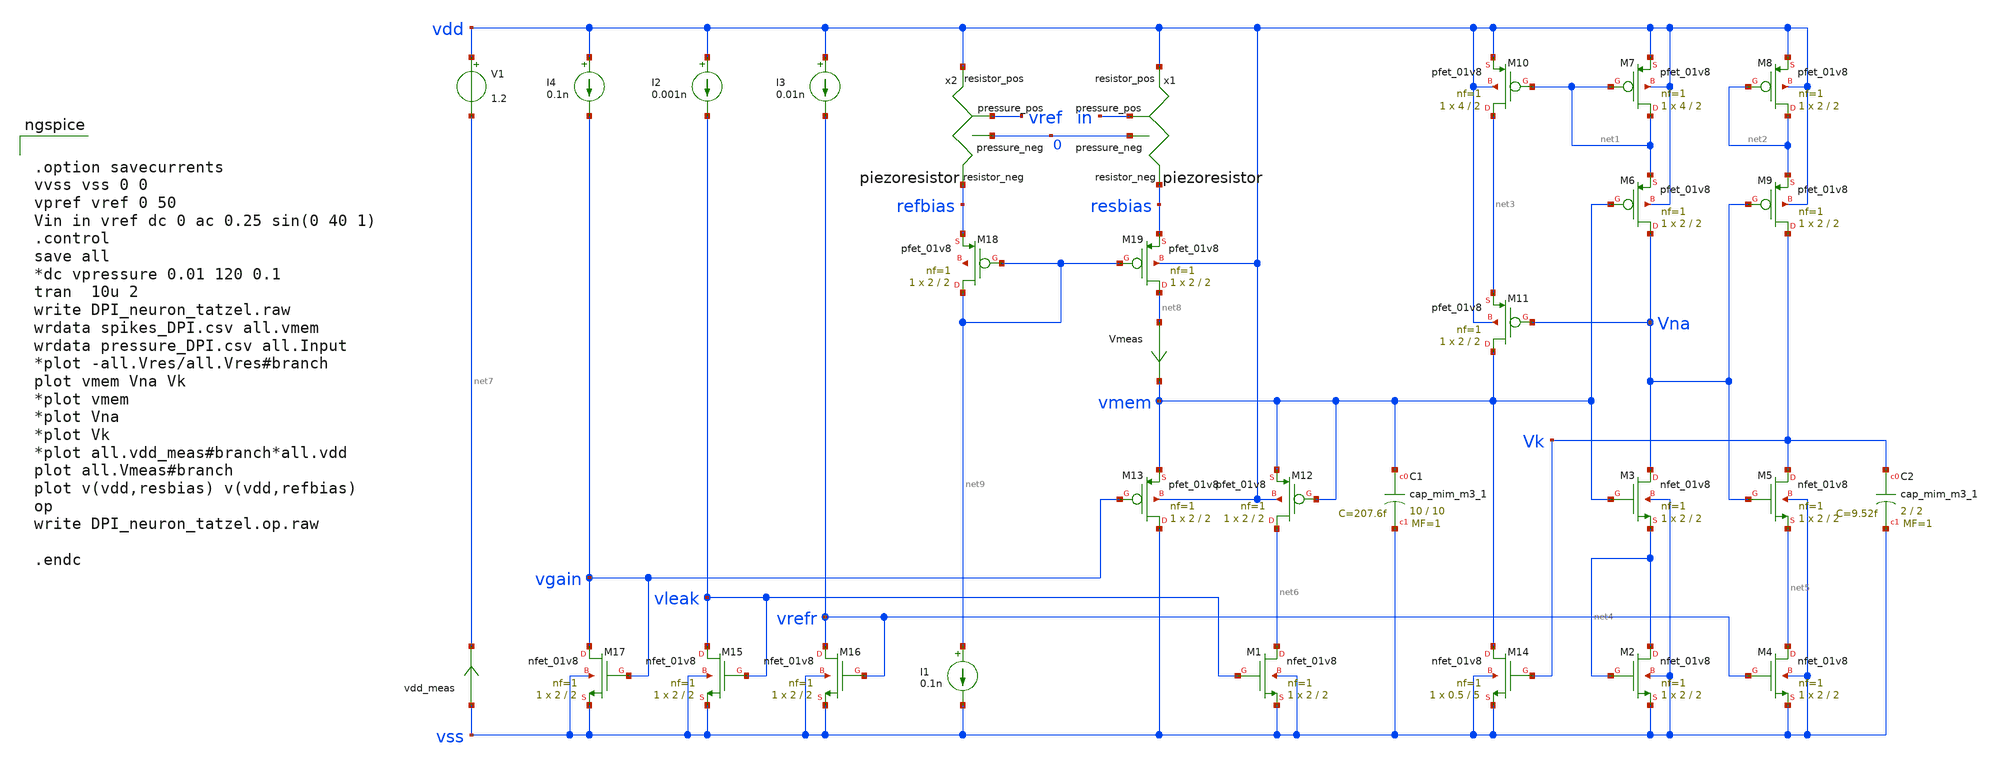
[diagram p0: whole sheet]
** sch_path: circuits/DPI_neuron_tatzel.sch
* Copyright 2020 Stefan Frederik Schippers
* Licensed under the Apache License, Version 2.0 (the "License");
* you may not use this file except in compliance with the License.
* You may obtain a copy of the License at
* https://www.apache.org/licenses/LICENSE-2.0
* Unless required by applicable law or agreed to in writing, software
* distributed under the License is distributed on an "AS IS" BASIS,
* WITHOUT WARRANTIES OR CONDITIONS OF ANY KIND, either express or implied.
* See the License for the specific language governing permissions and
* limitations under the License.
**.subckt DPI_neuron_tatzel
Vmeas net8 vmem 0
.save i(vmeas)
vdd_meas vss net7 0
.save i(vdd_meas)
V1 vdd net7 1.2
XM1 net6 vleak vss vss sky130_fd_pr__nfet_01v8 L=2 W=2 nf=1 ad='int((nf+1)/2) * W/nf * 0.29' as='int((nf+2)/2) * W/nf * 0.29'
+ pd='2*int((nf+1)/2) * (W/nf + 0.29)' ps='2*int((nf+2)/2) * (W/nf + 0.29)' nrd='0.29 / W' nrs='0.29 / W'
+ sa=0 sb=0 sd=0 mult=1 m=1
XM2 net4 net4 vss vss sky130_fd_pr__nfet_01v8 L=2 W=2 nf=1 ad='int((nf+1)/2) * W/nf * 0.29' as='int((nf+2)/2) * W/nf * 0.29'
+ pd='2*int((nf+1)/2) * (W/nf + 0.29)' ps='2*int((nf+2)/2) * (W/nf + 0.29)' nrd='0.29 / W' nrs='0.29 / W'
+ sa=0 sb=0 sd=0 mult=1 m=1
XM3 Vna vmem net4 vss sky130_fd_pr__nfet_01v8 L=2 W=2 nf=1 ad='int((nf+1)/2) * W/nf * 0.29' as='int((nf+2)/2) * W/nf * 0.29'
+ pd='2*int((nf+1)/2) * (W/nf + 0.29)' ps='2*int((nf+2)/2) * (W/nf + 0.29)' nrd='0.29 / W' nrs='0.29 / W'
+ sa=0 sb=0 sd=0 mult=1 m=1
XC1 vmem vss sky130_fd_pr__cap_mim_m3_1 W=10 L=10 MF=1 m=1
XC2 Vk vss sky130_fd_pr__cap_mim_m3_1 W=2 L=2 MF=1 m=1
XM14 vmem Vk vss vss sky130_fd_pr__nfet_01v8 L=5 W=0.5 nf=1 ad='int((nf+1)/2) * W/nf * 0.29' as='int((nf+2)/2) * W/nf * 0.29'
+ pd='2*int((nf+1)/2) * (W/nf + 0.29)' ps='2*int((nf+2)/2) * (W/nf + 0.29)' nrd='0.29 / W' nrs='0.29 / W'
+ sa=0 sb=0 sd=0 mult=1 m=1
XM4 net5 vrefr vss vss sky130_fd_pr__nfet_01v8 L=2 W=2 nf=1 ad='int((nf+1)/2) * W/nf * 0.29' as='int((nf+2)/2) * W/nf * 0.29'
+ pd='2*int((nf+1)/2) * (W/nf + 0.29)' ps='2*int((nf+2)/2) * (W/nf + 0.29)' nrd='0.29 / W' nrs='0.29 / W'
+ sa=0 sb=0 sd=0 mult=1 m=1
XM5 Vk Vna net5 vss sky130_fd_pr__nfet_01v8 L=2 W=2 nf=1 ad='int((nf+1)/2) * W/nf * 0.29' as='int((nf+2)/2) * W/nf * 0.29'
+ pd='2*int((nf+1)/2) * (W/nf + 0.29)' ps='2*int((nf+2)/2) * (W/nf + 0.29)' nrd='0.29 / W' nrs='0.29 / W'
+ sa=0 sb=0 sd=0 mult=1 m=1
I2 vdd vleak 0.001n
XM15 vleak vleak vss vss sky130_fd_pr__nfet_01v8 L=2 W=2 nf=1 ad='int((nf+1)/2) * W/nf * 0.29' as='int((nf+2)/2) * W/nf * 0.29'
+ pd='2*int((nf+1)/2) * (W/nf + 0.29)' ps='2*int((nf+2)/2) * (W/nf + 0.29)' nrd='0.29 / W' nrs='0.29 / W'
+ sa=0 sb=0 sd=0 mult=1 m=1
I3 vdd vrefr 0.01n
XM16 vrefr vrefr vss vss sky130_fd_pr__nfet_01v8 L=2 W=2 nf=1 ad='int((nf+1)/2) * W/nf * 0.29' as='int((nf+2)/2) * W/nf * 0.29'
+ pd='2*int((nf+1)/2) * (W/nf + 0.29)' ps='2*int((nf+2)/2) * (W/nf + 0.29)' nrd='0.29 / W' nrs='0.29 / W'
+ sa=0 sb=0 sd=0 mult=1 m=1
I4 vdd vgain 0.1n
XM17 vgain vgain vss vss sky130_fd_pr__nfet_01v8 L=2 W=2 nf=1 ad='int((nf+1)/2) * W/nf * 0.29' as='int((nf+2)/2) * W/nf * 0.29'
+ pd='2*int((nf+1)/2) * (W/nf + 0.29)' ps='2*int((nf+2)/2) * (W/nf + 0.29)' nrd='0.29 / W' nrs='0.29 / W'
+ sa=0 sb=0 sd=0 mult=1 m=1
XM6 Vna vmem net1 vdd sky130_fd_pr__pfet_01v8 L=2 W=2 nf=1 ad='int((nf+1)/2) * W/nf * 0.29' as='int((nf+2)/2) * W/nf * 0.29'
+ pd='2*int((nf+1)/2) * (W/nf + 0.29)' ps='2*int((nf+2)/2) * (W/nf + 0.29)' nrd='0.29 / W' nrs='0.29 / W'
+ sa=0 sb=0 sd=0 mult=1 m=1
XM7 net1 net1 vdd vdd sky130_fd_pr__pfet_01v8 L=2 W=4 nf=1 ad='int((nf+1)/2) * W/nf * 0.29' as='int((nf+2)/2) * W/nf * 0.29'
+ pd='2*int((nf+1)/2) * (W/nf + 0.29)' ps='2*int((nf+2)/2) * (W/nf + 0.29)' nrd='0.29 / W' nrs='0.29 / W'
+ sa=0 sb=0 sd=0 mult=1 m=1
XM8 net2 net2 vdd vdd sky130_fd_pr__pfet_01v8 L=2 W=2 nf=1 ad='int((nf+1)/2) * W/nf * 0.29' as='int((nf+2)/2) * W/nf * 0.29'
+ pd='2*int((nf+1)/2) * (W/nf + 0.29)' ps='2*int((nf+2)/2) * (W/nf + 0.29)' nrd='0.29 / W' nrs='0.29 / W'
+ sa=0 sb=0 sd=0 mult=1 m=1
XM9 Vk Vna net2 vdd sky130_fd_pr__pfet_01v8 L=2 W=2 nf=1 ad='int((nf+1)/2) * W/nf * 0.29' as='int((nf+2)/2) * W/nf * 0.29'
+ pd='2*int((nf+1)/2) * (W/nf + 0.29)' ps='2*int((nf+2)/2) * (W/nf + 0.29)' nrd='0.29 / W' nrs='0.29 / W'
+ sa=0 sb=0 sd=0 mult=1 m=1
XM10 net3 net1 vdd vdd sky130_fd_pr__pfet_01v8 L=2 W=4 nf=1 ad='int((nf+1)/2) * W/nf * 0.29' as='int((nf+2)/2) * W/nf * 0.29'
+ pd='2*int((nf+1)/2) * (W/nf + 0.29)' ps='2*int((nf+2)/2) * (W/nf + 0.29)' nrd='0.29 / W' nrs='0.29 / W'
+ sa=0 sb=0 sd=0 mult=1 m=1
XM11 vmem Vna net3 vdd sky130_fd_pr__pfet_01v8 L=2 W=2 nf=1 ad='int((nf+1)/2) * W/nf * 0.29' as='int((nf+2)/2) * W/nf * 0.29'
+ pd='2*int((nf+1)/2) * (W/nf + 0.29)' ps='2*int((nf+2)/2) * (W/nf + 0.29)' nrd='0.29 / W' nrs='0.29 / W'
+ sa=0 sb=0 sd=0 mult=1 m=1
XM12 net6 vmem vmem vdd sky130_fd_pr__pfet_01v8 L=2 W=2 nf=1 ad='int((nf+1)/2) * W/nf * 0.29' as='int((nf+2)/2) * W/nf * 0.29'
+ pd='2*int((nf+1)/2) * (W/nf + 0.29)' ps='2*int((nf+2)/2) * (W/nf + 0.29)' nrd='0.29 / W' nrs='0.29 / W'
+ sa=0 sb=0 sd=0 mult=1 m=1
XM13 vss vgain vmem vdd sky130_fd_pr__pfet_01v8 L=2 W=2 nf=1 ad='int((nf+1)/2) * W/nf * 0.29' as='int((nf+2)/2) * W/nf * 0.29'
+ pd='2*int((nf+1)/2) * (W/nf + 0.29)' ps='2*int((nf+2)/2) * (W/nf + 0.29)' nrd='0.29 / W' nrs='0.29 / W'
+ sa=0 sb=0 sd=0 mult=1 m=1
XM19 net8 net9 resbias vdd sky130_fd_pr__pfet_01v8 L=2 W=2 nf=1 ad='int((nf+1)/2) * W/nf * 0.29' as='int((nf+2)/2) * W/nf * 0.29'
+ pd='2*int((nf+1)/2) * (W/nf + 0.29)' ps='2*int((nf+2)/2) * (W/nf + 0.29)' nrd='0.29 / W' nrs='0.29 / W'
+ sa=0 sb=0 sd=0 mult=1 m=1
XM18 net9 net9 refbias net10 sky130_fd_pr__pfet_01v8 L=2 W=2 nf=1 ad='int((nf+1)/2) * W/nf * 0.29' as='int((nf+2)/2) * W/nf * 0.29'
+ pd='2*int((nf+1)/2) * (W/nf + 0.29)' ps='2*int((nf+2)/2) * (W/nf + 0.29)' nrd='0.29 / W' nrs='0.29 / W'
+ sa=0 sb=0 sd=0 mult=1 m=1
x1 in 0 vdd resbias piezoresistor
I1 net9 vss 0.1n
x2 vref 0 vdd refbias piezoresistor
**** begin user architecture code


.option savecurrents
vvss vss 0 0
vpref vref 0 50
Vin in vref dc 0 ac 0.25 sin(0 40 1)
.control
save all
*dc vpressure 0.01 120 0.1
tran  10u 2
write DPI_neuron_tatzel.raw
wrdata spikes_DPI.csv all.vmem
wrdata pressure_DPI.csv all.Input
*plot -all.Vres/all.Vres#branch
plot vmem Vna Vk
*plot vmem
*plot Vna
*plot Vk
*plot all.vdd_meas#branch*all.vdd
plot all.Vmeas#branch
plot v(vdd,resbias) v(vdd,refbias)
op
write DPI_neuron_tatzel.op.raw

.endc


 .lib $::SKYWATER_MODELS/models/sky130.lib.spice tt

.param mc_mm_switch=0
.param mc_pr_switch=1


**** end user architecture code
**.ends

* expanding   symbol:  /home/cmaier/.xschem/sky130_TAC3/circuits/piezoresistor.sym # of pins=4
** sym_path: circuits/piezoresistor.sym
** sch_path: circuits/piezoresistor.sch
.subckt piezoresistor pressure_pos pressure_neg resistor_pos resistor_neg
*.ipin pressure_pos
*.ipin pressure_neg
*.iopin resistor_pos
*.iopin resistor_neg
Broot sqrtp 0 V = sqrt(v(pressure_pos,pressure_neg))
Bres res 0 V = 106*(50/v(sqrtp)-1)*exp(-0.328*v(sqrtp))+15
Brvar resistor_pos resistor_neg I = V(resistor_pos,resistor_neg)/V(res)
.ends

.end
